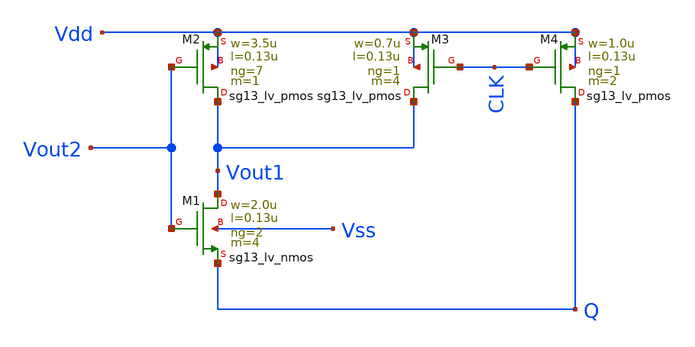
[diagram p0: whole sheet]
** sch_path: klayout/LVS/SA_upper.sch
**.subckt SA_upper
XM1 Vout1 Vout2 Q Vss sg13_lv_nmos w=2.0u l=0.13u ng=2 m=4 mm_ok=1
XM2 Vout1 Vout2 Vdd Vdd sg13_lv_pmos w=3.5u l=0.13u ng=7 m=1 mm_ok=1
XM3 Vout1 CLK Vdd Vdd sg13_lv_pmos w=0.7u l=0.13u ng=1 m=4 mm_ok=1
XM4 Q CLK Vdd Vdd sg13_lv_pmos w=1.0u l=0.13u ng=1 m=2 mm_ok=1
**.ends
.end
